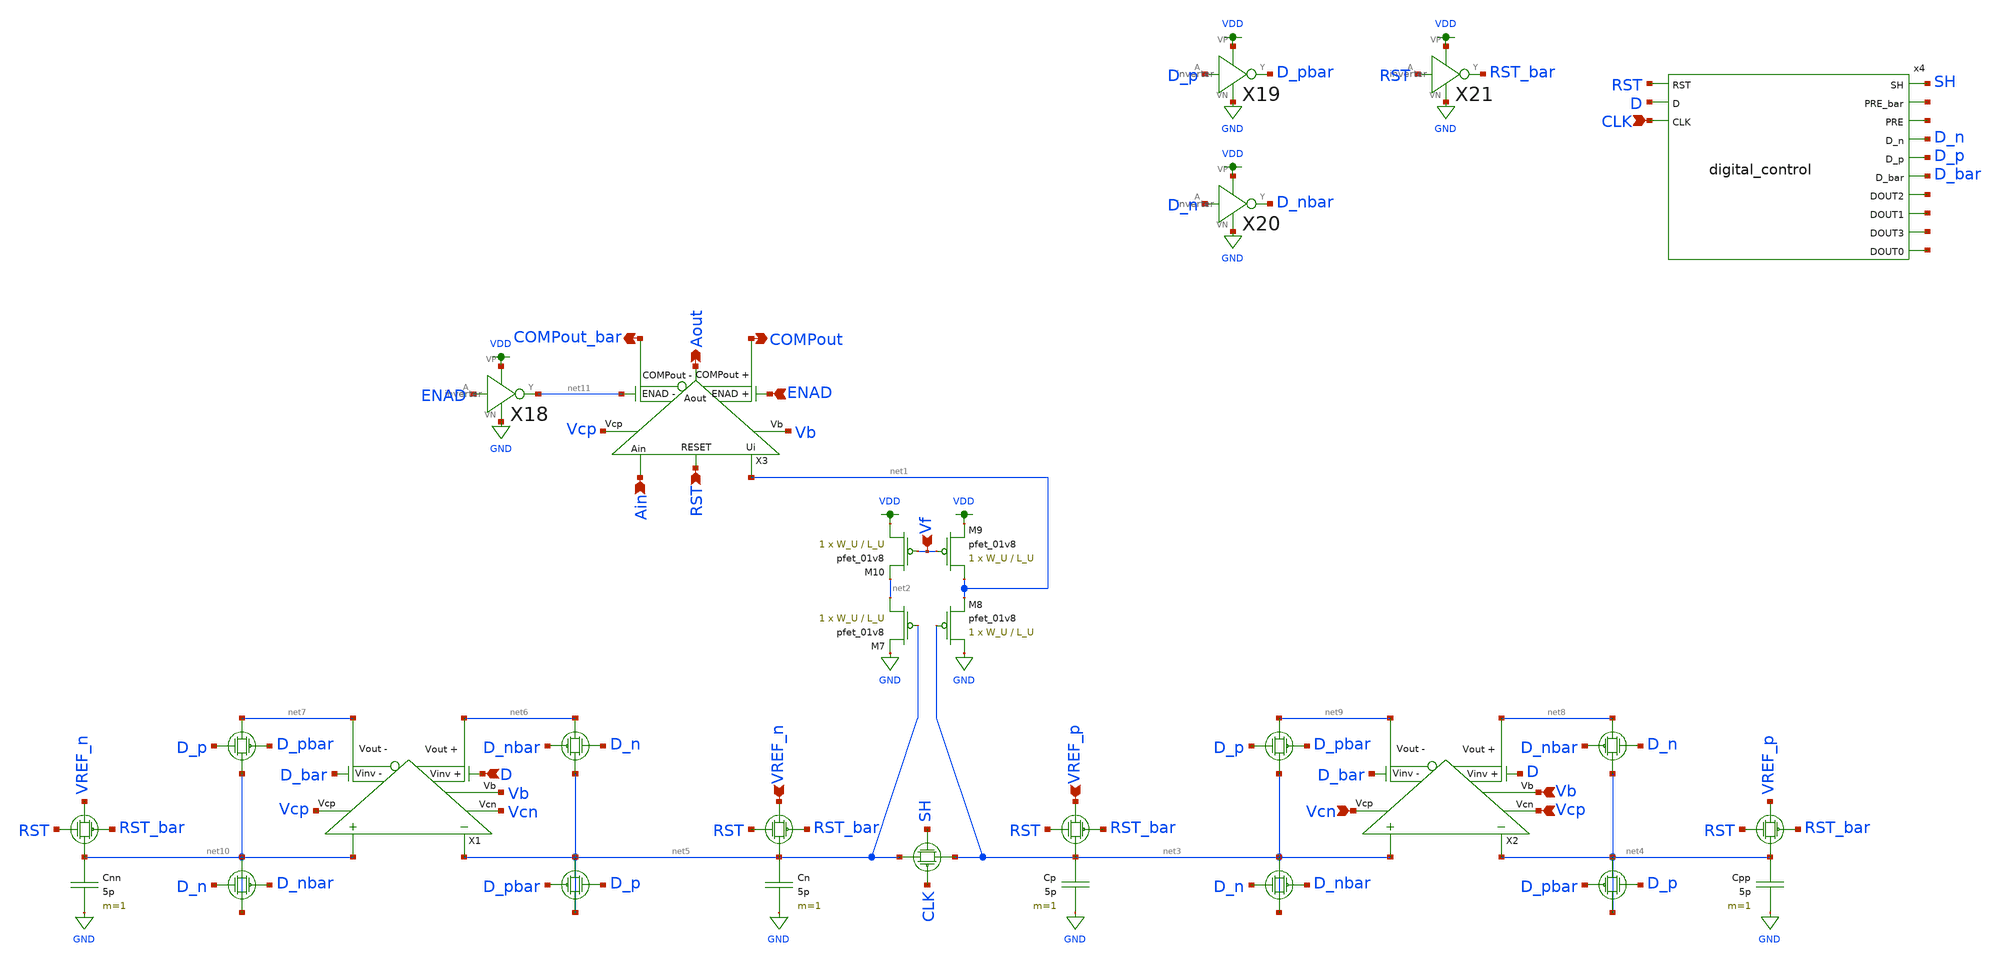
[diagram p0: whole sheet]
** sch_path: schematics/ada_converter.sch
**.subckt ada_converter Vcp RST Ain Aout COMPout_bar COMPout ENAD Vf D Vcn CLK VREF_p VREF_n Vb
*.ipin Vcp
*.ipin RST
*.ipin Ain
*.opin Aout
*.opin COMPout_bar
*.opin COMPout
*.ipin ENAD
*.ipin Vf
*.ipin D
*.ipin Vcn
*.ipin CLK
*.ipin VREF_p
*.ipin VREF_n
*.ipin Vb
X1 D_bar net6 net7 Vcp Vb net5 net10 D Vcn ota W_U=12 L_U=0.5
X2 D_bar net8 net9 Vcn Vb net4 net3 D Vcp ota W_U=12 L_U=0.5
X3 net11 COMPout_bar COMPout Vb net1 Ain ENAD Aout Vcp RST comp_pretty
Cp net3 GND 5p m=1
XM7 net2 net5 GND VDD sky130_fd_pr__pfet_01v8 L=L_U W=W_U nf=1 ad='int((nf+1)/2) * W/nf * 0.29' as='int((nf+2)/2) * W/nf * 0.29'
+ pd='2*int((nf+1)/2) * (W/nf + 0.29)' ps='2*int((nf+2)/2) * (W/nf + 0.29)' nrd='0.29 / W' nrs='0.29 / W'
+ sa=0 sb=0 sd=0 mult=1 m=1
XM8 GND net3 net1 VDD sky130_fd_pr__pfet_01v8 L=L_U W=W_U nf=1 ad='int((nf+1)/2) * W/nf * 0.29' as='int((nf+2)/2) * W/nf * 0.29'
+ pd='2*int((nf+1)/2) * (W/nf + 0.29)' ps='2*int((nf+2)/2) * (W/nf + 0.29)' nrd='0.29 / W' nrs='0.29 / W'
+ sa=0 sb=0 sd=0 mult=1 m=1
XM9 net1 Vf VDD VDD sky130_fd_pr__pfet_01v8 L=L_U W=W_U nf=1 ad='int((nf+1)/2) * W/nf * 0.29' as='int((nf+2)/2) * W/nf * 0.29'
+ pd='2*int((nf+1)/2) * (W/nf + 0.29)' ps='2*int((nf+2)/2) * (W/nf + 0.29)' nrd='0.29 / W' nrs='0.29 / W'
+ sa=0 sb=0 sd=0 mult=1 m=1
XM10 VDD Vf net2 VDD sky130_fd_pr__pfet_01v8 L=L_U W=W_U nf=1 ad='int((nf+1)/2) * W/nf * 0.29' as='int((nf+2)/2) * W/nf * 0.29'
+ pd='2*int((nf+1)/2) * (W/nf + 0.29)' ps='2*int((nf+2)/2) * (W/nf + 0.29)' nrd='0.29 / W' nrs='0.29 / W'
+ sa=0 sb=0 sd=0 mult=1 m=1
Cpp net4 GND 5p m=1
Cn net5 GND 5p m=1
Cnn net10 GND 5p m=1
x4 SH net12 RST net13 D_n D_p D_bar D net14 net15 net16 net17 CLK digital_control
X18 ENAD net11 VDD GND inverter
X19 D_p D_pbar VDD GND inverter
X20 D_n D_nbar VDD GND inverter
X21 RST RST_bar VDD GND inverter
**.ends

* expanding   symbol:  ../schematics/ota.sym # of pins=9
** sym_path: schematics/ota.sym
** sch_path: schematics/ota.sch
.subckt ota Vinv_n Vout_p Vout_n Vcp Vb Vin_n Vin_p Vinv_p Vcn  L_U=0.5 W_U=12
*.ipin Vin_n
*.ipin Vin_p
*.opin Vout_n
*.opin Vout_p
*.ipin Vcp
*.ipin Vb
*.ipin Vinv_p
*.ipin Vinv_n
*.ipin Vcn
XM18 net3 net3 VDD VDD sky130_fd_pr__pfet_01v8 L=L_U W=W_U nf=1 ad='int((nf+1)/2) * W/nf * 0.29' as='int((nf+2)/2) * W/nf * 0.29'
+ pd='2*int((nf+1)/2) * (W/nf + 0.29)' ps='2*int((nf+2)/2) * (W/nf + 0.29)' nrd='0.29 / W' nrs='0.29 / W'
+ sa=0 sb=0 sd=0 mult=1 m=1
XM19 net4 Vin_n net1 GND sky130_fd_pr__nfet_01v8 L=L_U W=W_U nf=1 ad='int((nf+1)/2) * W/nf * 0.29' as='int((nf+2)/2) * W/nf * 0.29'
+ pd='2*int((nf+1)/2) * (W/nf + 0.29)' ps='2*int((nf+2)/2) * (W/nf + 0.29)' nrd='0.29 / W' nrs='0.29 / W'
+ sa=0 sb=0 sd=0 mult=1 m=1
XM20 net3 Vin_p net1 GND sky130_fd_pr__nfet_01v8 L=L_U W=W_U nf=1 ad='int((nf+1)/2) * W/nf * 0.29' as='int((nf+2)/2) * W/nf * 0.29'
+ pd='2*int((nf+1)/2) * (W/nf + 0.29)' ps='2*int((nf+2)/2) * (W/nf + 0.29)' nrd='0.29 / W' nrs='0.29 / W'
+ sa=0 sb=0 sd=0 mult=1 m=1
XM21 net1 Vb GND GND sky130_fd_pr__nfet_01v8 L=L_U W=W_U nf=1 ad='int((nf+1)/2) * W/nf * 0.29' as='int((nf+2)/2) * W/nf * 0.29'
+ pd='2*int((nf+1)/2) * (W/nf + 0.29)' ps='2*int((nf+2)/2) * (W/nf + 0.29)' nrd='0.29 / W' nrs='0.29 / W'
+ sa=0 sb=0 sd=0 mult=1 m=1
XM22 net4 net4 VDD VDD sky130_fd_pr__pfet_01v8 L=L_U W=W_U nf=1 ad='int((nf+1)/2) * W/nf * 0.29' as='int((nf+2)/2) * W/nf * 0.29'
+ pd='2*int((nf+1)/2) * (W/nf + 0.29)' ps='2*int((nf+2)/2) * (W/nf + 0.29)' nrd='0.29 / W' nrs='0.29 / W'
+ sa=0 sb=0 sd=0 mult=1 m=1
XM23 net7 net3 VDD VDD sky130_fd_pr__pfet_01v8 L=L_U W=W_U nf=1 ad='int((nf+1)/2) * W/nf * 0.29' as='int((nf+2)/2) * W/nf * 0.29'
+ pd='2*int((nf+1)/2) * (W/nf + 0.29)' ps='2*int((nf+2)/2) * (W/nf + 0.29)' nrd='0.29 / W' nrs='0.29 / W'
+ sa=0 sb=0 sd=0 mult=1 m=1
XM24 net8 net4 VDD VDD sky130_fd_pr__pfet_01v8 L=L_U W=W_U nf=1 ad='int((nf+1)/2) * W/nf * 0.29' as='int((nf+2)/2) * W/nf * 0.29'
+ pd='2*int((nf+1)/2) * (W/nf + 0.29)' ps='2*int((nf+2)/2) * (W/nf + 0.29)' nrd='0.29 / W' nrs='0.29 / W'
+ sa=0 sb=0 sd=0 mult=1 m=1
XM25 net8 Vcp Vout_n VDD sky130_fd_pr__pfet_01v8 L=L_U W=W_U nf=1 ad='int((nf+1)/2) * W/nf * 0.29' as='int((nf+2)/2) * W/nf * 0.29'
+ pd='2*int((nf+1)/2) * (W/nf + 0.29)' ps='2*int((nf+2)/2) * (W/nf + 0.29)' nrd='0.29 / W' nrs='0.29 / W'
+ sa=0 sb=0 sd=0 mult=1 m=1
XM26 Vout_p Vcp net7 VDD sky130_fd_pr__pfet_01v8 L=L_U W=W_U nf=1 ad='int((nf+1)/2) * W/nf * 0.29' as='int((nf+2)/2) * W/nf * 0.29'
+ pd='2*int((nf+1)/2) * (W/nf + 0.29)' ps='2*int((nf+2)/2) * (W/nf + 0.29)' nrd='0.29 / W' nrs='0.29 / W'
+ sa=0 sb=0 sd=0 mult=1 m=1
XM27 Vout_p Vcn net6 GND sky130_fd_pr__nfet_01v8 L=L_U W=W_U nf=1 ad='int((nf+1)/2) * W/nf * 0.29' as='int((nf+2)/2) * W/nf * 0.29'
+ pd='2*int((nf+1)/2) * (W/nf + 0.29)' ps='2*int((nf+2)/2) * (W/nf + 0.29)' nrd='0.29 / W' nrs='0.29 / W'
+ sa=0 sb=0 sd=0 mult=1 m=1
XM28 Vout_n Vcn net2 GND sky130_fd_pr__nfet_01v8 L=L_U W=W_U nf=1 ad='int((nf+1)/2) * W/nf * 0.29' as='int((nf+2)/2) * W/nf * 0.29'
+ pd='2*int((nf+1)/2) * (W/nf + 0.29)' ps='2*int((nf+2)/2) * (W/nf + 0.29)' nrd='0.29 / W' nrs='0.29 / W'
+ sa=0 sb=0 sd=0 mult=1 m=1
XM29 net6 net5 GND GND sky130_fd_pr__nfet_01v8 L=L_U W=W_U nf=1 ad='int((nf+1)/2) * W/nf * 0.29' as='int((nf+2)/2) * W/nf * 0.29'
+ pd='2*int((nf+1)/2) * (W/nf + 0.29)' ps='2*int((nf+2)/2) * (W/nf + 0.29)' nrd='0.29 / W' nrs='0.29 / W'
+ sa=0 sb=0 sd=0 mult=1 m=1
XM30 Vout_p Vinv_p net5 GND sky130_fd_pr__nfet_01v8 L=L_U W=W_U nf=1 ad='int((nf+1)/2) * W/nf * 0.29'
+ as='int((nf+2)/2) * W/nf * 0.29' pd='2*int((nf+1)/2) * (W/nf + 0.29)' ps='2*int((nf+2)/2) * (W/nf + 0.29)'
+ nrd='0.29 / W' nrs='0.29 / W' sa=0 sb=0 sd=0 mult=1 m=1
XM32 net2 net5 GND GND sky130_fd_pr__nfet_01v8 L=L_U W=W_U nf=1 ad='int((nf+1)/2) * W/nf * 0.29' as='int((nf+2)/2) * W/nf * 0.29'
+ pd='2*int((nf+1)/2) * (W/nf + 0.29)' ps='2*int((nf+2)/2) * (W/nf + 0.29)' nrd='0.29 / W' nrs='0.29 / W'
+ sa=0 sb=0 sd=0 mult=1 m=1
XM34 Vout_n Vinv_n net5 GND sky130_fd_pr__nfet_01v8 L=L_U W=W_U nf=1 ad='int((nf+1)/2) * W/nf * 0.29'
+ as='int((nf+2)/2) * W/nf * 0.29' pd='2*int((nf+1)/2) * (W/nf + 0.29)' ps='2*int((nf+2)/2) * (W/nf + 0.29)'
+ nrd='0.29 / W' nrs='0.29 / W' sa=0 sb=0 sd=0 mult=1 m=1
.ends


* expanding   symbol:  ../schematics/comp_pretty.sym # of pins=10
** sym_path: schematics/comp_pretty.sym
** sch_path: schematics/comp_pretty.sch
.subckt comp_pretty ENAD_n COMPout_n COMPout_p Vb Ui Ain ENAD_p Aout Vcp RST
*.ipin Ain
*.ipin Vcp
*.ipin Vb
*.opin Aout
*.opin COMPout_n
*.opin COMPout_p
*.ipin ENAD_n
*.ipin RST
*.ipin Ui
*.ipin ENAD_p
XM1 net1 net1 VDD VDD sky130_fd_pr__pfet_01v8 L=L_U W=W_U nf=1 ad='int((nf+1)/2) * W/nf * 0.29' as='int((nf+2)/2) * W/nf * 0.29'
+ pd='2*int((nf+1)/2) * (W/nf + 0.29)' ps='2*int((nf+2)/2) * (W/nf + 0.29)' nrd='0.29 / W' nrs='0.29 / W'
+ sa=0 sb=0 sd=0 mult=1 m=1
XM2 net2 Ain net5 GND sky130_fd_pr__nfet_01v8 L=L_U W=W_U nf=1 ad='int((nf+1)/2) * W/nf * 0.29' as='int((nf+2)/2) * W/nf * 0.29'
+ pd='2*int((nf+1)/2) * (W/nf + 0.29)' ps='2*int((nf+2)/2) * (W/nf + 0.29)' nrd='0.29 / W' nrs='0.29 / W'
+ sa=0 sb=0 sd=0 mult=1 m=1
XM3 net1 Ui net5 GND sky130_fd_pr__nfet_01v8 L=L_U W=W_U nf=1 ad='int((nf+1)/2) * W/nf * 0.29' as='int((nf+2)/2) * W/nf * 0.29'
+ pd='2*int((nf+1)/2) * (W/nf + 0.29)' ps='2*int((nf+2)/2) * (W/nf + 0.29)' nrd='0.29 / W' nrs='0.29 / W'
+ sa=0 sb=0 sd=0 mult=1 m=1
XM4 net5 Vb GND GND sky130_fd_pr__nfet_01v8 L=L_U W=W_U nf=1 ad='int((nf+1)/2) * W/nf * 0.29' as='int((nf+2)/2) * W/nf * 0.29'
+ pd='2*int((nf+1)/2) * (W/nf + 0.29)' ps='2*int((nf+2)/2) * (W/nf + 0.29)' nrd='0.29 / W' nrs='0.29 / W'
+ sa=0 sb=0 sd=0 mult=1 m=1
XM5 net2 net2 VDD VDD sky130_fd_pr__pfet_01v8 L=L_U W=W_U nf=1 ad='int((nf+1)/2) * W/nf * 0.29' as='int((nf+2)/2) * W/nf * 0.29'
+ pd='2*int((nf+1)/2) * (W/nf + 0.29)' ps='2*int((nf+2)/2) * (W/nf + 0.29)' nrd='0.29 / W' nrs='0.29 / W'
+ sa=0 sb=0 sd=0 mult=1 m=1
XM6 net8 net1 VDD VDD sky130_fd_pr__pfet_01v8 L=L_U W=W_U nf=1 ad='int((nf+1)/2) * W/nf * 0.29' as='int((nf+2)/2) * W/nf * 0.29'
+ pd='2*int((nf+1)/2) * (W/nf + 0.29)' ps='2*int((nf+2)/2) * (W/nf + 0.29)' nrd='0.29 / W' nrs='0.29 / W'
+ sa=0 sb=0 sd=0 mult=1 m=1
XM7 net9 net2 VDD VDD sky130_fd_pr__pfet_01v8 L=L_U W=W_U nf=1 ad='int((nf+1)/2) * W/nf * 0.29' as='int((nf+2)/2) * W/nf * 0.29'
+ pd='2*int((nf+1)/2) * (W/nf + 0.29)' ps='2*int((nf+2)/2) * (W/nf + 0.29)' nrd='0.29 / W' nrs='0.29 / W'
+ sa=0 sb=0 sd=0 mult=1 m=1
XM8 net9 Vcp COMPout_p VDD sky130_fd_pr__pfet_01v8 L=L_U W=W_U nf=1 ad='int((nf+1)/2) * W/nf * 0.29'
+ as='int((nf+2)/2) * W/nf * 0.29' pd='2*int((nf+1)/2) * (W/nf + 0.29)' ps='2*int((nf+2)/2) * (W/nf + 0.29)'
+ nrd='0.29 / W' nrs='0.29 / W' sa=0 sb=0 sd=0 mult=1 m=1
XM9 COMPout_n Vcp net8 VDD sky130_fd_pr__pfet_01v8 L=L_U W=W_U nf=1 ad='int((nf+1)/2) * W/nf * 0.29'
+ as='int((nf+2)/2) * W/nf * 0.29' pd='2*int((nf+1)/2) * (W/nf + 0.29)' ps='2*int((nf+2)/2) * (W/nf + 0.29)'
+ nrd='0.29 / W' nrs='0.29 / W' sa=0 sb=0 sd=0 mult=1 m=1
XM10 net1 Vb GND GND sky130_fd_pr__nfet_01v8 L=L_U W=W_U nf=1 ad='int((nf+1)/2) * W/nf * 0.29' as='int((nf+2)/2) * W/nf * 0.29'
+ pd='2*int((nf+1)/2) * (W/nf + 0.29)' ps='2*int((nf+2)/2) * (W/nf + 0.29)' nrd='0.29 / W' nrs='0.29 / W'
+ sa=0 sb=0 sd=0 mult=1 m=1
XM11 net2 Vb GND GND sky130_fd_pr__nfet_01v8 L=L_U W=W_U nf=1 ad='int((nf+1)/2) * W/nf * 0.29' as='int((nf+2)/2) * W/nf * 0.29'
+ pd='2*int((nf+1)/2) * (W/nf + 0.29)' ps='2*int((nf+2)/2) * (W/nf + 0.29)' nrd='0.29 / W' nrs='0.29 / W'
+ sa=0 sb=0 sd=0 mult=1 m=1
XM12 COMPout_n net6 net4 GND sky130_fd_pr__nfet_01v8 L=L_U W=W_U nf=1 ad='int((nf+1)/2) * W/nf * 0.29'
+ as='int((nf+2)/2) * W/nf * 0.29' pd='2*int((nf+1)/2) * (W/nf + 0.29)' ps='2*int((nf+2)/2) * (W/nf + 0.29)'
+ nrd='0.29 / W' nrs='0.29 / W' sa=0 sb=0 sd=0 mult=1 m=1
XM13 net6 ENAD_n VDD VDD sky130_fd_pr__pfet_01v8 L=L_U W=W_U nf=1 ad='int((nf+1)/2) * W/nf * 0.29' as='int((nf+2)/2) * W/nf * 0.29'
+ pd='2*int((nf+1)/2) * (W/nf + 0.29)' ps='2*int((nf+2)/2) * (W/nf + 0.29)' nrd='0.29 / W' nrs='0.29 / W'
+ sa=0 sb=0 sd=0 mult=1 m=1
XM14 COMPout_p net6 net3 GND sky130_fd_pr__nfet_01v8 L=L_U W=W_U nf=1 ad='int((nf+1)/2) * W/nf * 0.29'
+ as='int((nf+2)/2) * W/nf * 0.29' pd='2*int((nf+1)/2) * (W/nf + 0.29)' ps='2*int((nf+2)/2) * (W/nf + 0.29)'
+ nrd='0.29 / W' nrs='0.29 / W' sa=0 sb=0 sd=0 mult=1 m=1
XM15 COMPout_p ENAD_n net6 GND sky130_fd_pr__nfet_01v8 L=L_U W=W_U nf=1 ad='int((nf+1)/2) * W/nf * 0.29'
+ as='int((nf+2)/2) * W/nf * 0.29' pd='2*int((nf+1)/2) * (W/nf + 0.29)' ps='2*int((nf+2)/2) * (W/nf + 0.29)'
+ nrd='0.29 / W' nrs='0.29 / W' sa=0 sb=0 sd=0 mult=1 m=1
XM16 net4 net3 GND GND sky130_fd_pr__nfet_01v8 L=L_U W=W_U nf=1 ad='int((nf+1)/2) * W/nf * 0.29' as='int((nf+2)/2) * W/nf * 0.29'
+ pd='2*int((nf+1)/2) * (W/nf + 0.29)' ps='2*int((nf+2)/2) * (W/nf + 0.29)' nrd='0.29 / W' nrs='0.29 / W'
+ sa=0 sb=0 sd=0 mult=1 m=1
XM17 net3 net7 GND GND sky130_fd_pr__nfet_01v8 L=L_U W=W_U nf=1 ad='int((nf+1)/2) * W/nf * 0.29' as='int((nf+2)/2) * W/nf * 0.29'
+ pd='2*int((nf+1)/2) * (W/nf + 0.29)' ps='2*int((nf+2)/2) * (W/nf + 0.29)' nrd='0.29 / W' nrs='0.29 / W'
+ sa=0 sb=0 sd=0 mult=1 m=1
XM18 net7 ENAD_n net3 GND sky130_fd_pr__nfet_01v8 L=L_U W=W_U nf=1 ad='int((nf+1)/2) * W/nf * 0.29' as='int((nf+2)/2) * W/nf * 0.29'
+ pd='2*int((nf+1)/2) * (W/nf + 0.29)' ps='2*int((nf+2)/2) * (W/nf + 0.29)' nrd='0.29 / W' nrs='0.29 / W'
+ sa=0 sb=0 sd=0 mult=1 m=1
XM19 net4 ENAD_p net7 GND sky130_fd_pr__nfet_01v8 L=L_U W=W_U nf=1 ad='int((nf+1)/2) * W/nf * 0.29' as='int((nf+2)/2) * W/nf * 0.29'
+ pd='2*int((nf+1)/2) * (W/nf + 0.29)' ps='2*int((nf+2)/2) * (W/nf + 0.29)' nrd='0.29 / W' nrs='0.29 / W'
+ sa=0 sb=0 sd=0 mult=1 m=1
XM20 net7 RST net3 GND sky130_fd_pr__nfet_01v8 L=L_U W=W_U nf=1 ad='int((nf+1)/2) * W/nf * 0.29' as='int((nf+2)/2) * W/nf * 0.29'
+ pd='2*int((nf+1)/2) * (W/nf + 0.29)' ps='2*int((nf+2)/2) * (W/nf + 0.29)' nrd='0.29 / W' nrs='0.29 / W'
+ sa=0 sb=0 sd=0 mult=1 m=1
C1 net3 GND 1p m=1
C2 net7 GND 1p m=1
XM26 Aout ENAD_p COMPout_n VDD sky130_fd_pr__pfet_01v8 L=L_U W=W_U nf=1 ad='int((nf+1)/2) * W/nf * 0.29'
+ as='int((nf+2)/2) * W/nf * 0.29' pd='2*int((nf+1)/2) * (W/nf + 0.29)' ps='2*int((nf+2)/2) * (W/nf + 0.29)'
+ nrd='0.29 / W' nrs='0.29 / W' sa=0 sb=0 sd=0 mult=1 m=1
XM21 Aout ENAD_n COMPout_n GND sky130_fd_pr__nfet_01v8 L=L_U W=W_U nf=1 ad='int((nf+1)/2) * W/nf * 0.29'
+ as='int((nf+2)/2) * W/nf * 0.29' pd='2*int((nf+1)/2) * (W/nf + 0.29)' ps='2*int((nf+2)/2) * (W/nf + 0.29)'
+ nrd='0.29 / W' nrs='0.29 / W' sa=0 sb=0 sd=0 mult=1 m=1
.ends


* expanding   symbol:  ../schematics/digital_control.sym # of pins=13
** sym_path: schematics/digital_control.sym
** sch_path: schematics/digital_control.sch
.subckt digital_control SH PRE_bar RST PRE D_n D_p D_bar D DOUT2 DOUT1 DOUT3 DOUT0 CLK
*.ipin D
*.opin D_bar
*.opin PRE_bar
*.opin SH
*.opin DOUT0
*.opin DOUT1
*.opin DOUT2
*.opin DOUT3
*.ipin CLK
*.opin PRE
*.ipin RST
*.opin D_p
*.opin D_n
X2 PRE_bar PRE VDD GND inverter
X9 CLK SH VDD GND inverter
X1 D D_bar VDD GND inverter
X7 D net4 VDD GND inverter
x3 CLK DOUT0 D net1 net4 CRSL_edge_sens
x4 CLK DOUT1 DOUT0 net2 net1 CRSL_edge_sens
x5 CLK DOUT2 DOUT1 net3 net2 CRSL_edge_sens
x6 CLK DOUT3 DOUT2 net7 net3 CRSL_edge_sens
x11 VDD D net5 CLK GND nand2
X12 net5 D_p VDD GND inverter
x14 VDD D_bar net6 CLK GND nand2
X15 net6 D_n VDD GND inverter
x8 VDD CLK PRE_bar RST GND nand2
.ends


* expanding   symbol:  ../schematics/inverter.sym # of pins=4
** sym_path: schematics/inverter.sym
** sch_path: schematics/inverter.sch
.subckt inverter A Y VP VN
*.ipin A
*.iopin VP
*.iopin VN
*.opin Y
XM1 Y A VP VDD sky130_fd_pr__pfet_01v8 L=0.15 W=1 nf=1 ad='int((nf+1)/2) * W/nf * 0.29' as='int((nf+2)/2) * W/nf * 0.29'
+ pd='2*int((nf+1)/2) * (W/nf + 0.29)' ps='2*int((nf+2)/2) * (W/nf + 0.29)' nrd='0.29 / W' nrs='0.29 / W'
+ sa=0 sb=0 sd=0 mult=1 m=1
XM2 Y A VN GND sky130_fd_pr__nfet_01v8 L=0.15 W=1 nf=1 ad='int((nf+1)/2) * W/nf * 0.29' as='int((nf+2)/2) * W/nf * 0.29'
+ pd='2*int((nf+1)/2) * (W/nf + 0.29)' ps='2*int((nf+2)/2) * (W/nf + 0.29)' nrd='0.29 / W' nrs='0.29 / W'
+ sa=0 sb=0 sd=0 mult=1 m=1
.ends


* expanding   symbol:  ../schematics/CRSL_edge_sens.sym # of pins=5
** sym_path: schematics/CRSL_edge_sens.sym
** sch_path: schematics/CRSL_edge_sens.sch
.subckt CRSL_edge_sens Phi Q D Q_bar D_bar
*.ipin D
*.ipin D_bar
*.opin Q
*.opin Q_bar
*.ipin Phi
XM14 Q_bar Q GND GND sky130_fd_pr__nfet_01v8 L=0.15 W=1 nf=1 ad='int((nf+1)/2) * W/nf * 0.29' as='int((nf+2)/2) * W/nf * 0.29'
+ pd='2*int((nf+1)/2) * (W/nf + 0.29)' ps='2*int((nf+2)/2) * (W/nf + 0.29)' nrd='0.29 / W' nrs='0.29 / W'
+ sa=0 sb=0 sd=0 mult=1 m=1
XM2 Q_bar Phi net3 GND sky130_fd_pr__nfet_01v8 L=0.15 W=1 nf=1 ad='int((nf+1)/2) * W/nf * 0.29' as='int((nf+2)/2) * W/nf * 0.29'
+ pd='2*int((nf+1)/2) * (W/nf + 0.29)' ps='2*int((nf+2)/2) * (W/nf + 0.29)' nrd='0.29 / W' nrs='0.29 / W'
+ sa=0 sb=0 sd=0 mult=1 m=1
XM6 Q Phi net2 GND sky130_fd_pr__nfet_01v8 L=0.15 W=1 nf=1 ad='int((nf+1)/2) * W/nf * 0.29' as='int((nf+2)/2) * W/nf * 0.29'
+ pd='2*int((nf+1)/2) * (W/nf + 0.29)' ps='2*int((nf+2)/2) * (W/nf + 0.29)' nrd='0.29 / W' nrs='0.29 / W'
+ sa=0 sb=0 sd=0 mult=1 m=1
XM7 net4 Phi GND GND sky130_fd_pr__nfet_01v8 L=0.15 W=4 nf=1 ad='int((nf+1)/2) * W/nf * 0.29' as='int((nf+2)/2) * W/nf * 0.29'
+ pd='2*int((nf+1)/2) * (W/nf + 0.29)' ps='2*int((nf+2)/2) * (W/nf + 0.29)' nrd='0.29 / W' nrs='0.29 / W'
+ sa=0 sb=0 sd=0 mult=1 m=1
XM8 net3 net2 net4 GND sky130_fd_pr__nfet_01v8 L=0.15 W=1 nf=1 ad='int((nf+1)/2) * W/nf * 0.29' as='int((nf+2)/2) * W/nf * 0.29'
+ pd='2*int((nf+1)/2) * (W/nf + 0.29)' ps='2*int((nf+2)/2) * (W/nf + 0.29)' nrd='0.29 / W' nrs='0.29 / W'
+ sa=0 sb=0 sd=0 mult=1 m=1
XM12 net3 net2 VDD VDD sky130_fd_pr__pfet_01v8 L=0.15 W=1 nf=1 ad='int((nf+1)/2) * W/nf * 0.29' as='int((nf+2)/2) * W/nf * 0.29'
+ pd='2*int((nf+1)/2) * (W/nf + 0.29)' ps='2*int((nf+2)/2) * (W/nf + 0.29)' nrd='0.29 / W' nrs='0.29 / W'
+ sa=0 sb=0 sd=0 mult=1 m=1
XM9 net2 net3 VDD VDD sky130_fd_pr__pfet_01v8 L=0.15 W=1 nf=1 ad='int((nf+1)/2) * W/nf * 0.29' as='int((nf+2)/2) * W/nf * 0.29'
+ pd='2*int((nf+1)/2) * (W/nf + 0.29)' ps='2*int((nf+2)/2) * (W/nf + 0.29)' nrd='0.29 / W' nrs='0.29 / W'
+ sa=0 sb=0 sd=0 mult=1 m=1
XM1 net1 Phi VDD VDD sky130_fd_pr__pfet_01v8 L=0.15 W=4 nf=1 ad='int((nf+1)/2) * W/nf * 0.29' as='int((nf+2)/2) * W/nf * 0.29'
+ pd='2*int((nf+1)/2) * (W/nf + 0.29)' ps='2*int((nf+2)/2) * (W/nf + 0.29)' nrd='0.29 / W' nrs='0.29 / W'
+ sa=0 sb=0 sd=0 mult=1 m=1
XM3 Q_bar Q net1 VDD sky130_fd_pr__pfet_01v8 L=0.15 W=1 nf=1 ad='int((nf+1)/2) * W/nf * 0.29' as='int((nf+2)/2) * W/nf * 0.29'
+ pd='2*int((nf+1)/2) * (W/nf + 0.29)' ps='2*int((nf+2)/2) * (W/nf + 0.29)' nrd='0.29 / W' nrs='0.29 / W'
+ sa=0 sb=0 sd=0 mult=1 m=1
XM4 Q Q_bar net1 VDD sky130_fd_pr__pfet_01v8 L=0.15 W=1 nf=1 ad='int((nf+1)/2) * W/nf * 0.29' as='int((nf+2)/2) * W/nf * 0.29'
+ pd='2*int((nf+1)/2) * (W/nf + 0.29)' ps='2*int((nf+2)/2) * (W/nf + 0.29)' nrd='0.29 / W' nrs='0.29 / W'
+ sa=0 sb=0 sd=0 mult=1 m=1
XM10 Q Q_bar GND GND sky130_fd_pr__nfet_01v8 L=0.15 W=1 nf=1 ad='int((nf+1)/2) * W/nf * 0.29' as='int((nf+2)/2) * W/nf * 0.29'
+ pd='2*int((nf+1)/2) * (W/nf + 0.29)' ps='2*int((nf+2)/2) * (W/nf + 0.29)' nrd='0.29 / W' nrs='0.29 / W'
+ sa=0 sb=0 sd=0 mult=1 m=1
XM5 net2 net3 net4 GND sky130_fd_pr__nfet_01v8 L=0.15 W=1 nf=1 ad='int((nf+1)/2) * W/nf * 0.29' as='int((nf+2)/2) * W/nf * 0.29'
+ pd='2*int((nf+1)/2) * (W/nf + 0.29)' ps='2*int((nf+2)/2) * (W/nf + 0.29)' nrd='0.29 / W' nrs='0.29 / W'
+ sa=0 sb=0 sd=0 mult=1 m=1
XM11 net3 Phi D_bar VDD sky130_fd_pr__pfet_01v8 L=0.15 W=1 nf=1 ad='int((nf+1)/2) * W/nf * 0.29' as='int((nf+2)/2) * W/nf * 0.29'
+ pd='2*int((nf+1)/2) * (W/nf + 0.29)' ps='2*int((nf+2)/2) * (W/nf + 0.29)' nrd='0.29 / W' nrs='0.29 / W'
+ sa=0 sb=0 sd=0 mult=1 m=1
XM15 net2 Phi D VDD sky130_fd_pr__pfet_01v8 L=0.15 W=1 nf=1 ad='int((nf+1)/2) * W/nf * 0.29' as='int((nf+2)/2) * W/nf * 0.29'
+ pd='2*int((nf+1)/2) * (W/nf + 0.29)' ps='2*int((nf+2)/2) * (W/nf + 0.29)' nrd='0.29 / W' nrs='0.29 / W'
+ sa=0 sb=0 sd=0 mult=1 m=1
.ends


* expanding   symbol:  /home/madvlsi/algorithmic-ada-converter/schematics/nand2.sym # of pins=5
** sym_path: schematics/nand2.sym
** sch_path: schematics/nand2.sch
.subckt nand2 VP B Y A VN
*.iopin VP
*.iopin VN
*.ipin A
*.ipin B
*.opin Y
XM5 Y B VP VP sky130_fd_pr__pfet_01v8 L=0.15 W=1 nf=1 ad='int((nf+1)/2) * W/nf * 0.29' as='int((nf+2)/2) * W/nf * 0.29'
+ pd='2*int((nf+1)/2) * (W/nf + 0.29)' ps='2*int((nf+2)/2) * (W/nf + 0.29)' nrd='0.29 / W' nrs='0.29 / W'
+ sa=0 sb=0 sd=0 mult=1 m=1
XM2 Y A VP VP sky130_fd_pr__pfet_01v8 L=0.15 W=1 nf=1 ad='int((nf+1)/2) * W/nf * 0.29' as='int((nf+2)/2) * W/nf * 0.29'
+ pd='2*int((nf+1)/2) * (W/nf + 0.29)' ps='2*int((nf+2)/2) * (W/nf + 0.29)' nrd='0.29 / W' nrs='0.29 / W'
+ sa=0 sb=0 sd=0 mult=1 m=1
XM1 Y A net1 VN sky130_fd_pr__nfet_01v8 L=0.15 W=1 nf=1 ad='int((nf+1)/2) * W/nf * 0.29' as='int((nf+2)/2) * W/nf * 0.29'
+ pd='2*int((nf+1)/2) * (W/nf + 0.29)' ps='2*int((nf+2)/2) * (W/nf + 0.29)' nrd='0.29 / W' nrs='0.29 / W'
+ sa=0 sb=0 sd=0 mult=1 m=1
XM3 net1 B VN VN sky130_fd_pr__nfet_01v8 L=0.15 W=1 nf=1 ad='int((nf+1)/2) * W/nf * 0.29' as='int((nf+2)/2) * W/nf * 0.29'
+ pd='2*int((nf+1)/2) * (W/nf + 0.29)' ps='2*int((nf+2)/2) * (W/nf + 0.29)' nrd='0.29 / W' nrs='0.29 / W'
+ sa=0 sb=0 sd=0 mult=1 m=1
.ends

.GLOBAL GND
.GLOBAL VDD
.end
